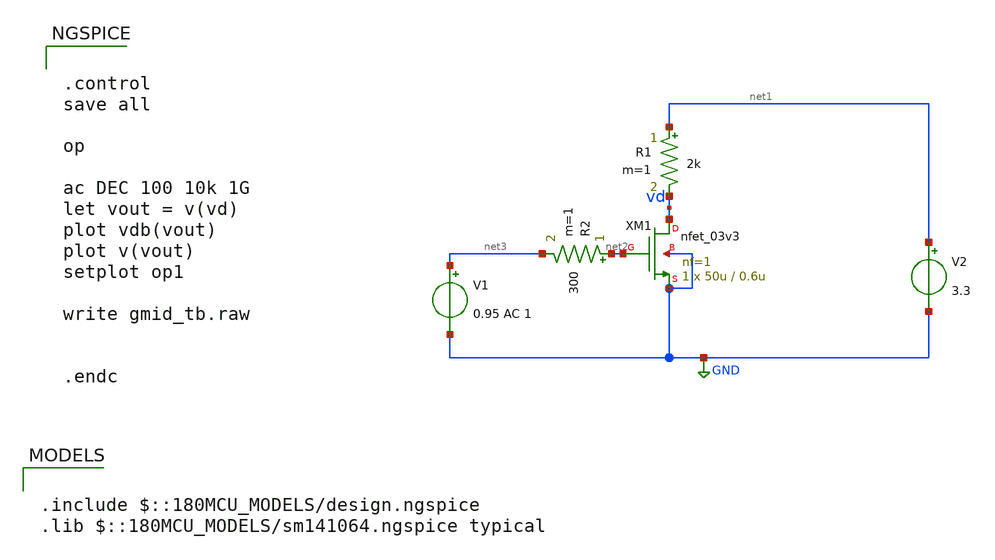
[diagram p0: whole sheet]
** sch_path: designs/libs/tb_analog/unit_transistors/gmid_tb.sch
**.subckt gmid_tb
XM1 vd net2 GND GND nfet_03v3 L=0.6u W=50u nf=1 ad='int((nf+1)/2) * W/nf * 0.18u' as='int((nf+2)/2) * W/nf * 0.18u'
+ pd='2*int((nf+1)/2) * (W/nf + 0.18u)' ps='2*int((nf+2)/2) * (W/nf + 0.18u)' nrd='0.18u / W' nrs='0.18u / W'
+ sa=0 sb=0 sd=0 m=1
V1 net3 GND 0.95 AC 1
V2 net1 GND 3.3
R1 net1 vd 2k m=1
R2 net2 net3 300 m=1
**** begin user architecture code

.include $::180MCU_MODELS/design.ngspice
.lib $::180MCU_MODELS/sm141064.ngspice typical



.control
save all

op

ac DEC 100 10k 1G
let vout = v(vd)
plot vdb(vout)
plot v(vout)
setplot op1

write gmid_tb.raw


.endc


**** end user architecture code
**.ends
.GLOBAL GND
.end
